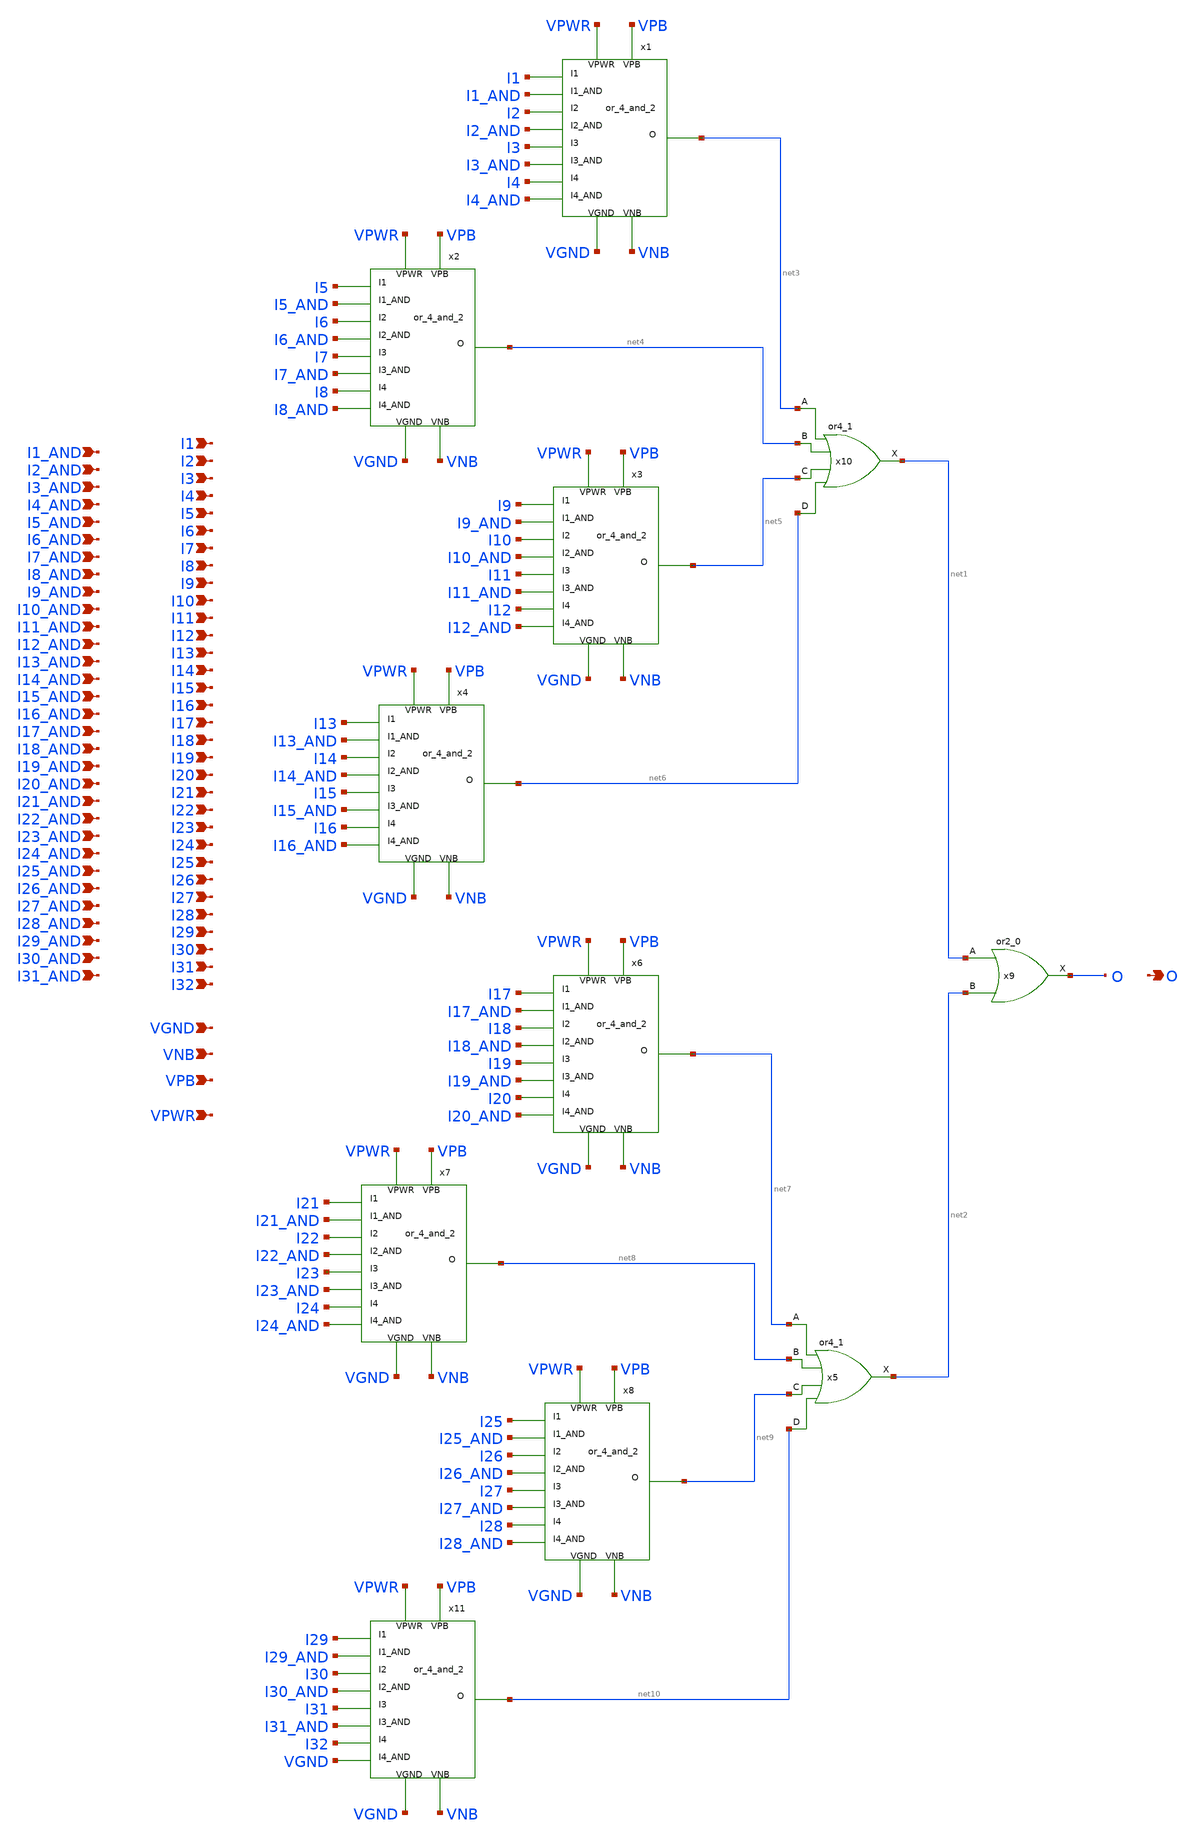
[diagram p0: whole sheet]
** sch_path: schematics/or_32.sch
**.subckt or_32 I1 I2 I12 I3 I4 I5 I6 I7 I8 I9 I10 I11 I13 I14 I15 I16 I17 I18 I19 I20 I21 I22 I23
*+ I24 I25 I26 I27 I28 I29 I30 I31 I32 O VGND VNB VPB VPWR I1_AND I2_AND I12_AND I3_AND I4_AND I5_AND
*+ I6_AND I7_AND I8_AND I9_AND I10_AND I11_AND I13_AND I14_AND I15_AND I16_AND I17_AND I18_AND I19_AND
*+ I20_AND I21_AND I22_AND I23_AND I24_AND I25_AND I26_AND I27_AND I28_AND I29_AND I30_AND I31_AND
*.ipin I1
*.ipin I2
*.ipin I12
*.ipin I3
*.ipin I4
*.ipin I5
*.ipin I6
*.ipin I7
*.ipin I8
*.ipin I9
*.ipin I10
*.ipin I11
*.ipin I13
*.ipin I14
*.ipin I15
*.ipin I16
*.ipin I17
*.ipin I18
*.ipin I19
*.ipin I20
*.ipin I21
*.ipin I22
*.ipin I23
*.ipin I24
*.ipin I25
*.ipin I26
*.ipin I27
*.ipin I28
*.ipin I29
*.ipin I30
*.ipin I31
*.ipin I32
*.opin O
*.ipin VGND
*.ipin VNB
*.ipin VPB
*.ipin VPWR
*.ipin I1_AND
*.ipin I2_AND
*.ipin I12_AND
*.ipin I3_AND
*.ipin I4_AND
*.ipin I5_AND
*.ipin I6_AND
*.ipin I7_AND
*.ipin I8_AND
*.ipin I9_AND
*.ipin I10_AND
*.ipin I11_AND
*.ipin I13_AND
*.ipin I14_AND
*.ipin I15_AND
*.ipin I16_AND
*.ipin I17_AND
*.ipin I18_AND
*.ipin I19_AND
*.ipin I20_AND
*.ipin I21_AND
*.ipin I22_AND
*.ipin I23_AND
*.ipin I24_AND
*.ipin I25_AND
*.ipin I26_AND
*.ipin I27_AND
*.ipin I28_AND
*.ipin I29_AND
*.ipin I30_AND
*.ipin I31_AND
x10 net3 net4 net5 net6 VGND VNB VPB VPWR net1 sky130_fd_sc_hd__or4_1
x9 net1 net2 VGND VNB VPB VPWR O sky130_fd_sc_hd__or2_0
x1 I1 I1_AND I2 I2_AND I3 I3_AND I4 I4_AND VPWR VPB VGND VNB net3 or_4_and_2
x2 I5 I5_AND I6 I6_AND I7 I7_AND I8 I8_AND VPWR VPB VGND VNB net4 or_4_and_2
x3 I9 I9_AND I10 I10_AND I11 I11_AND I12 I12_AND VPWR VPB VGND VNB net5 or_4_and_2
x4 I13 I13_AND I14 I14_AND I15 I15_AND I16 I16_AND VPWR VPB VGND VNB net6 or_4_and_2
x5 net7 net8 net9 net10 VGND VNB VPB VPWR net2 sky130_fd_sc_hd__or4_1
x6 I17 I17_AND I18 I18_AND I19 I19_AND I20 I20_AND VPWR VPB VGND VNB net7 or_4_and_2
x7 I21 I21_AND I22 I22_AND I23 I23_AND I24 I24_AND VPWR VPB VGND VNB net8 or_4_and_2
x8 I25 I25_AND I26 I26_AND I27 I27_AND I28 I28_AND VPWR VPB VGND VNB net9 or_4_and_2
x11 I29 I29_AND I30 I30_AND I31 I31_AND I32 VGND VPWR VPB VGND VNB net10 or_4_and_2
**.ends

* expanding   symbol:  schematics/or_4_and_2.sym # of pins=13
** sym_path: schematics/or_4_and_2.sym
** sch_path: schematics/or_4_and_2.sch
.subckt or_4_and_2 I1 I1_AND I2 I2_AND I3 I3_AND I4 I4_AND VPWR VPB VGND VNB O
*.opin O
*.ipin I1
*.ipin I2
*.ipin I3
*.ipin I4
*.ipin I1_AND
*.ipin I2_AND
*.ipin I3_AND
*.ipin I4_AND
*.ipin VGND
*.ipin VNB
*.ipin VPB
*.ipin VPWR
x1 net3 net1 net4 net2 VGND VNB VPB VPWR O sky130_fd_sc_hd__or4_1
x2 I2 net5 VGND VNB VPB VPWR net1 sky130_fd_sc_hd__and2_0
x3 I1 net6 VGND VNB VPB VPWR net3 sky130_fd_sc_hd__and2_0
x4 I4 net7 VGND VNB VPB VPWR net2 sky130_fd_sc_hd__and2_0
x5 I3 net8 VGND VNB VPB VPWR net4 sky130_fd_sc_hd__and2_0
x6 I2_AND VGND VNB VPB VPWR net5 sky130_fd_sc_hd__inv_1
x7 I1_AND VGND VNB VPB VPWR net6 sky130_fd_sc_hd__inv_1
x8 I3_AND VGND VNB VPB VPWR net8 sky130_fd_sc_hd__inv_1
x9 I4_AND VGND VNB VPB VPWR net7 sky130_fd_sc_hd__inv_1
.ends

.end
